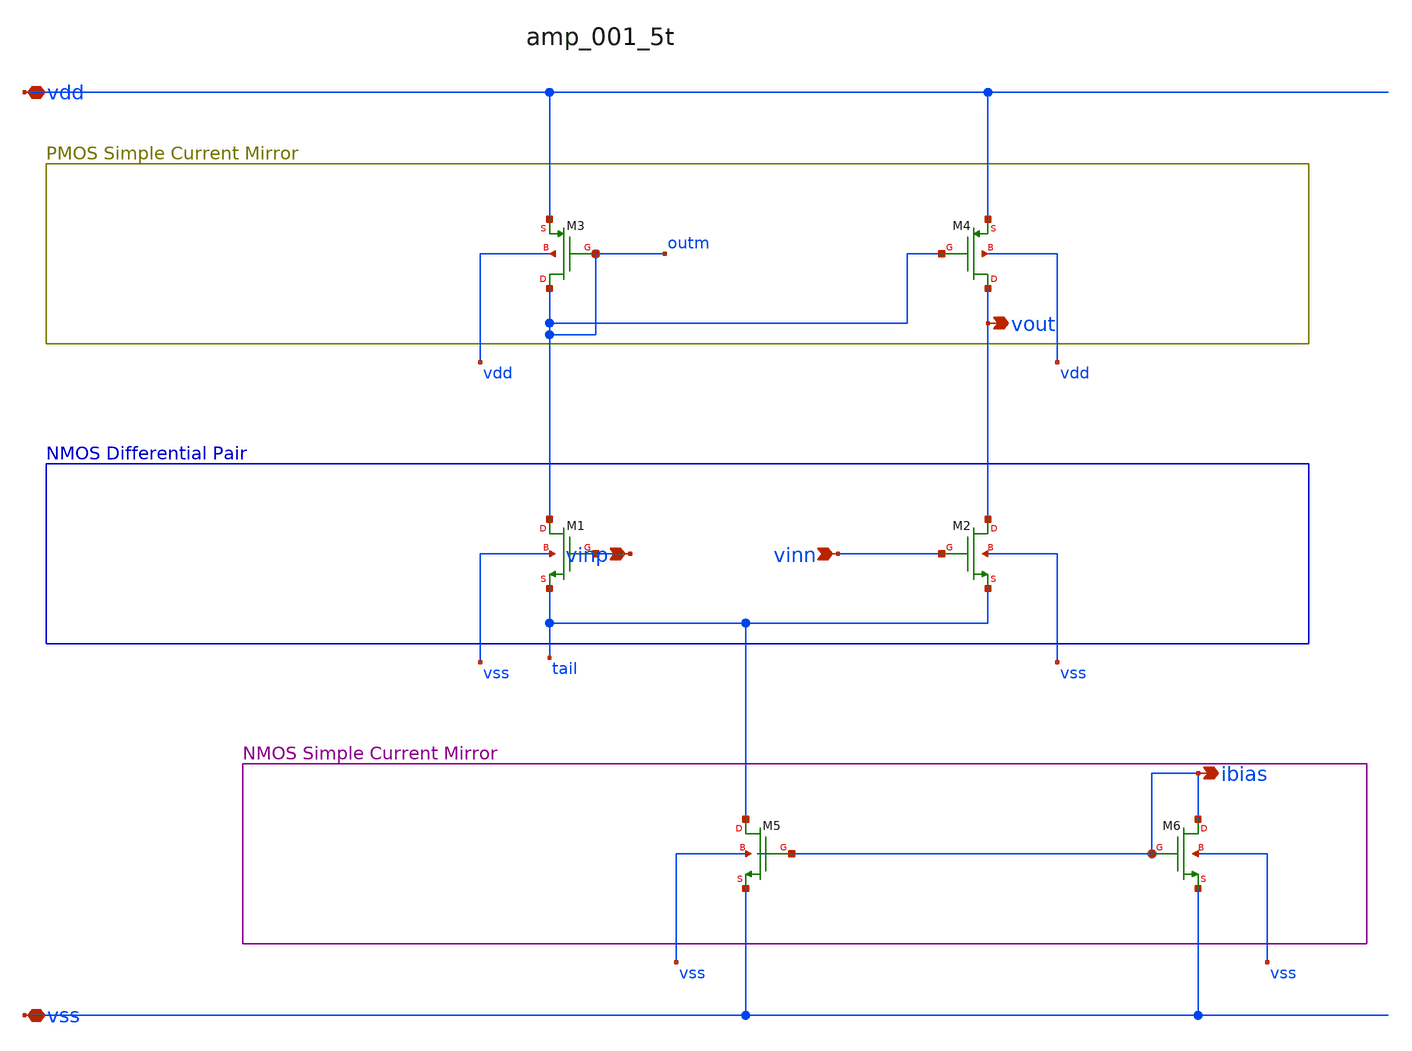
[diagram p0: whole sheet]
** sch_path: analog-db/raw/amp_001_5t/amp_001_5t_annotated.sch
**.subckt amp_001_5t_annotated vinp vinn vdd vss vout ibias
*.ipin vinp
*.ipin vinn
*.iopin vdd
*.iopin vss
*.opin vout
*.opin ibias
XM1 outm vinp tail vss sg13_lv_nmos w=x_dut_xm1_w l=x_dut_xm1_l ng=1 m=x_dut_xm1_m
XM2 vout vinn tail vss sg13_lv_nmos w=x_dut_xm2_w l=x_dut_xm2_l ng=1 m=x_dut_xm2_m
XM3 outm outm vdd vdd sg13_lv_pmos w=x_dut_xm3_w l=x_dut_xm3_l ng=1 m=x_dut_xm3_m
XM4 vout outm vdd vdd sg13_lv_pmos w=x_dut_xm4_w l=x_dut_xm4_l ng=1 m=x_dut_xm4_m
XM5 tail ibias vss vss sg13_lv_nmos w=x_dut_xm5_w l=x_dut_xm5_l ng=1 m=x_dut_xm5_m
XM6 ibias ibias vss vss sg13_lv_nmos w=x_dut_xm6_w l=x_dut_xm6_l ng=1 m=x_dut_xm6_m
**.ends
.end
